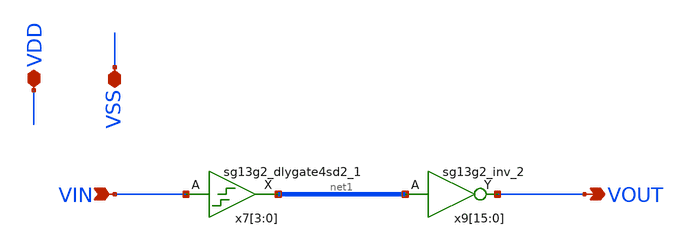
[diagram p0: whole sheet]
** sch_path: Cells/DLine.sch
* IHP-GmbH/IHP-Open-PDK/ihp-sg13g2/libs.tech/xschem/sg13g2_stdcells/sg13g2_dlygate4sd2_1.sch:
* Copyright 2023 IHP PDK Authors
* Licensed under the Apache License, Version 2.0 (the "License");
**.subckt DLine VOUT VIN VDD VSS
*.opin VOUT
*.ipin VIN
*.iopin VDD
*.iopin VSS
x7[3] net1[3] VIN VDD VSS sg13g2_dlygate4sd2_1
x7[2] net1[2] VIN VDD VSS sg13g2_dlygate4sd2_1
x7[1] net1[1] VIN VDD VSS sg13g2_dlygate4sd2_1
x7[0] net1[0] VIN VDD VSS sg13g2_dlygate4sd2_1
x9[15] VOUT net1[3] VDD VSS sg13g2_inv_2
x9[14] VOUT net1[2] VDD VSS sg13g2_inv_2
x9[13] VOUT net1[1] VDD VSS sg13g2_inv_2
x9[12] VOUT net1[0] VDD VSS sg13g2_inv_2
x9[11] VOUT net1[3] VDD VSS sg13g2_inv_2
x9[10] VOUT net1[2] VDD VSS sg13g2_inv_2
x9[9] VOUT net1[1] VDD VSS sg13g2_inv_2
x9[8] VOUT net1[0] VDD VSS sg13g2_inv_2
x9[7] VOUT net1[3] VDD VSS sg13g2_inv_2
x9[6] VOUT net1[2] VDD VSS sg13g2_inv_2
x9[5] VOUT net1[1] VDD VSS sg13g2_inv_2
x9[4] VOUT net1[0] VDD VSS sg13g2_inv_2
x9[3] VOUT net1[3] VDD VSS sg13g2_inv_2
x9[2] VOUT net1[2] VDD VSS sg13g2_inv_2
x9[1] VOUT net1[1] VDD VSS sg13g2_inv_2
x9[0] VOUT net1[0] VDD VSS sg13g2_inv_2
**.ends

* expanding   symbol:  sg13g2_stdcells/sg13g2_dlygate4sd2_1.sym # of pins=2
** sym_path: sg13g2_stdcells/sg13g2_dlygate4sd2_1.sym
** sch_path: sg13g2_stdcells/sg13g2_dlygate4sd2_1.sch
.subckt sg13g2_dlygate4sd2_1 X A VDD VSS
*.ipin A
*.opin X
*.iopin VDD
*.iopin VSS
XM1 net2 A VSS VSS sg13_lv_nmos w=420.00n l=130.00n ng=1 m=1 mm_ok=1
XM2 net1 net2 VSS VSS sg13_lv_nmos w=420.00n l=180.00n ng=1 m=1 mm_ok=1
XM3 net3 net1 VSS VSS sg13_lv_nmos w=420.00n l=180.00n ng=1 m=1 mm_ok=1
XM4 X net3 VSS VSS sg13_lv_nmos w=740.00n l=130.00n ng=1 m=1 mm_ok=1
XM5 net2 A VDD VDD sg13_lv_pmos w=420.00n l=130.00n ng=1 m=1 mm_ok=1
XM6 net1 net2 VDD VDD sg13_lv_pmos w=1.000u l=250.00n ng=1 m=1 mm_ok=1
XM7 net3 net1 VDD VDD sg13_lv_pmos w=1.000u l=250.00n ng=1 m=1 mm_ok=1
XM8 X net3 VDD VDD sg13_lv_pmos w=1.12u l=130.00n ng=1 m=1 mm_ok=1
.ends


* expanding   symbol:  sg13g2_stdcells/sg13g2_inv_2.sym # of pins=2
** sym_path: sg13g2_stdcells/sg13g2_inv_2.sym
** sch_path: sg13g2_stdcells/sg13g2_inv_2.sch
.subckt sg13g2_inv_2 Y A VDD VSS
*.opin Y
*.ipin A
*.iopin VDD
*.iopin VSS
XM1 Y A VSS VSS sg13_lv_nmos w=1.48u l=130.00n ng=2 m=1 mm_ok=1
XM2 Y A VDD VDD sg13_lv_pmos w=2.24u l=130.00n ng=2 m=1 mm_ok=1
.ends

.end
